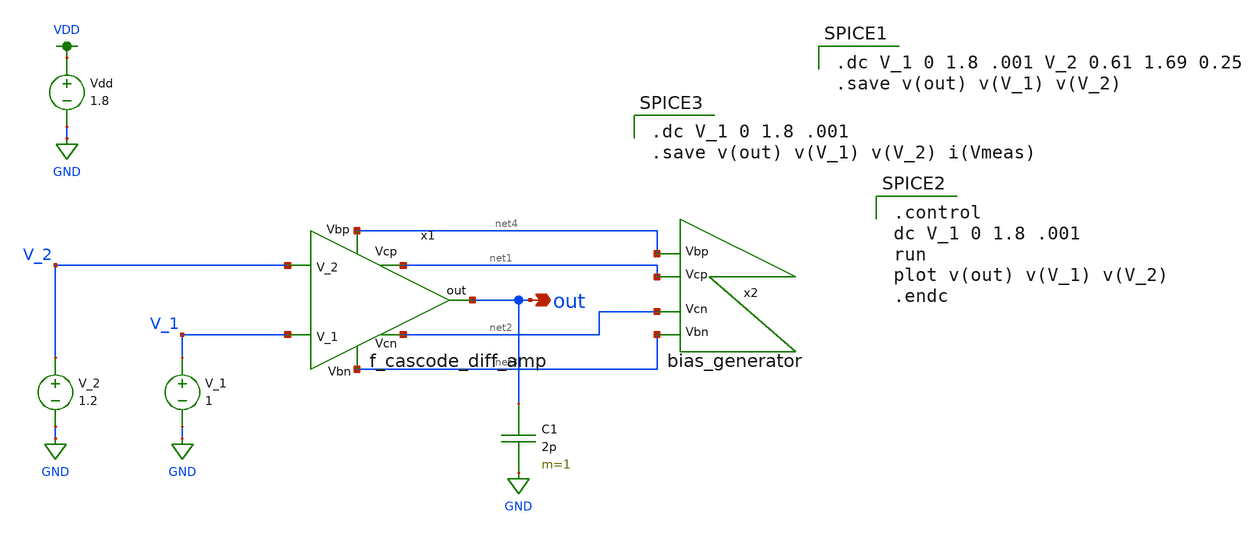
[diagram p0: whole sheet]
** sch_path: miniproject3/test_harness.sch
**.subckt test_harness out
*.opin out
x1 net4 net1 V_2 out V_1 net2 net3 f_cascode_diff_amp
x2 net4 net1 net2 net3 bias_generator
Vdd VDD GND 1.8
V_2 V_2 GND 1.2
V_1 V_1 GND 1
C1 out GND 2p m=1
**** begin user architecture code

.dc V_1 0 1.8 .001 V_2 0.61 1.69 0.25
.save v(out) v(V_1) v(V_2)


.option wnflag=1
.lib ~/skywater/skywater-pdk/libraries/sky130_fd_pr_ngspice/latest/models/sky130.lib.spice tt


.control
dc V_1 0 1.8 .001
run
plot v(out) v(V_1) v(V_2)
.endc


.dc V_1 0 1.8 .001
.save v(out) v(V_1) v(V_2) i(Vmeas)

**** end user architecture code
**.ends

* expanding   symbol:  /home/lxbtlr/MAD/miniproject3/f_cascode_diff_amp.sym # of pins=7
** sym_path: miniproject3/f_cascode_diff_amp.sym
** sch_path: miniproject3/f_cascode_diff_amp.sch
.subckt f_cascode_diff_amp Vbp Vcp V_2 out V_1 Vcn Vbn
*.ipin V_1
*.ipin V_2
*.ipin Vcp
*.ipin Vcn
*.opin out
*.ipin Vbp
*.ipin Vbn
XM11 net4 V_2 net6 GND sky130_fd_pr__nfet_01v8 L=0.5 W=12 nf=1 ad='int((nf+1)/2) * W/nf * 0.29' as='int((nf+2)/2) * W/nf * 0.29'
+ pd='2*int((nf+1)/2) * (W/nf + 0.29)' ps='2*int((nf+2)/2) * (W/nf + 0.29)' nrd='0.29 / W' nrs='0.29 / W'
+ sa=0 sb=0 sd=0 mult=1 m=1
XM10 net5 V_1 net6 GND sky130_fd_pr__nfet_01v8 L=0.5 W=12 nf=1 ad='int((nf+1)/2) * W/nf * 0.29' as='int((nf+2)/2) * W/nf * 0.29'
+ pd='2*int((nf+1)/2) * (W/nf + 0.29)' ps='2*int((nf+2)/2) * (W/nf + 0.29)' nrd='0.29 / W' nrs='0.29 / W'
+ sa=0 sb=0 sd=0 mult=1 m=1
XM1 net6 Vbn GND GND sky130_fd_pr__nfet_01v8 L=0.5 W=12 nf=1 ad='int((nf+1)/2) * W/nf * 0.29' as='int((nf+2)/2) * W/nf * 0.29'
+ pd='2*int((nf+1)/2) * (W/nf + 0.29)' ps='2*int((nf+2)/2) * (W/nf + 0.29)' nrd='0.29 / W' nrs='0.29 / W'
+ sa=0 sb=0 sd=0 mult=1 m=1
XM8 GND net2 net1 GND sky130_fd_pr__nfet_01v8 L=0.5 W=12 nf=1 ad='int((nf+1)/2) * W/nf * 0.29' as='int((nf+2)/2) * W/nf * 0.29'
+ pd='2*int((nf+1)/2) * (W/nf + 0.29)' ps='2*int((nf+2)/2) * (W/nf + 0.29)' nrd='0.29 / W' nrs='0.29 / W'
+ sa=0 sb=0 sd=0 mult=1 m=1
XM9 net3 net2 GND GND sky130_fd_pr__nfet_01v8 L=0.5 W=12 nf=1 ad='int((nf+1)/2) * W/nf * 0.29' as='int((nf+2)/2) * W/nf * 0.29'
+ pd='2*int((nf+1)/2) * (W/nf + 0.29)' ps='2*int((nf+2)/2) * (W/nf + 0.29)' nrd='0.29 / W' nrs='0.29 / W'
+ sa=0 sb=0 sd=0 mult=1 m=1
XM7 out Vcn net3 GND sky130_fd_pr__nfet_01v8 L=0.5 W=12 nf=1 ad='int((nf+1)/2) * W/nf * 0.29' as='int((nf+2)/2) * W/nf * 0.29'
+ pd='2*int((nf+1)/2) * (W/nf + 0.29)' ps='2*int((nf+2)/2) * (W/nf + 0.29)' nrd='0.29 / W' nrs='0.29 / W'
+ sa=0 sb=0 sd=0 mult=1 m=1
XM2 net2 Vcn net1 GND sky130_fd_pr__nfet_01v8 L=0.5 W=12 nf=1 ad='int((nf+1)/2) * W/nf * 0.29' as='int((nf+2)/2) * W/nf * 0.29'
+ pd='2*int((nf+1)/2) * (W/nf + 0.29)' ps='2*int((nf+2)/2) * (W/nf + 0.29)' nrd='0.29 / W' nrs='0.29 / W'
+ sa=0 sb=0 sd=0 mult=1 m=1
XM5 net2 Vcp net5 VDD sky130_fd_pr__pfet_01v8 L=0.5 W=12 nf=1 ad='int((nf+1)/2) * W/nf * 0.29' as='int((nf+2)/2) * W/nf * 0.29'
+ pd='2*int((nf+1)/2) * (W/nf + 0.29)' ps='2*int((nf+2)/2) * (W/nf + 0.29)' nrd='0.29 / W' nrs='0.29 / W'
+ sa=0 sb=0 sd=0 mult=1 m=1
XM6 out Vcp net4 VDD sky130_fd_pr__pfet_01v8 L=0.5 W=12 nf=1 ad='int((nf+1)/2) * W/nf * 0.29' as='int((nf+2)/2) * W/nf * 0.29'
+ pd='2*int((nf+1)/2) * (W/nf + 0.29)' ps='2*int((nf+2)/2) * (W/nf + 0.29)' nrd='0.29 / W' nrs='0.29 / W'
+ sa=0 sb=0 sd=0 mult=1 m=1
XM4 net4 Vbp VDD VDD sky130_fd_pr__pfet_01v8 L=0.5 W=12 nf=1 ad='int((nf+1)/2) * W/nf * 0.29' as='int((nf+2)/2) * W/nf * 0.29'
+ pd='2*int((nf+1)/2) * (W/nf + 0.29)' ps='2*int((nf+2)/2) * (W/nf + 0.29)' nrd='0.29 / W' nrs='0.29 / W'
+ sa=0 sb=0 sd=0 mult=1 m=1
XM3 net5 Vbp VDD VDD sky130_fd_pr__pfet_01v8 L=0.5 W=12 nf=1 ad='int((nf+1)/2) * W/nf * 0.29' as='int((nf+2)/2) * W/nf * 0.29'
+ pd='2*int((nf+1)/2) * (W/nf + 0.29)' ps='2*int((nf+2)/2) * (W/nf + 0.29)' nrd='0.29 / W' nrs='0.29 / W'
+ sa=0 sb=0 sd=0 mult=1 m=1
.ends


* expanding   symbol:  /home/lxbtlr/MAD/miniproject3/bias_generator.sym # of pins=4
** sym_path: miniproject3/bias_generator.sym
** sch_path: miniproject3/bias_generator.sch
.subckt bias_generator Vbp Vcp Vcn Vbn
*.opin Vbp
*.opin Vbn
*.opin Vcp
*.opin Vcn
XM1 net2 Vbp VDD VDD sky130_fd_pr__pfet_01v8 L=2.5 W=12 nf=1 ad='int((nf+1)/2) * W/nf * 0.29' as='int((nf+2)/2) * W/nf * 0.29'
+ pd='2*int((nf+1)/2) * (W/nf + 0.29)' ps='2*int((nf+2)/2) * (W/nf + 0.29)' nrd='0.29 / W' nrs='0.29 / W'
+ sa=0 sb=0 sd=0 mult=1 m=1
XM2 Vcn Vbp VDD VDD sky130_fd_pr__pfet_01v8 L=0.5 W=12 nf=1 ad='int((nf+1)/2) * W/nf * 0.29' as='int((nf+2)/2) * W/nf * 0.29'
+ pd='2*int((nf+1)/2) * (W/nf + 0.29)' ps='2*int((nf+2)/2) * (W/nf + 0.29)' nrd='0.29 / W' nrs='0.29 / W'
+ sa=0 sb=0 sd=0 mult=1 m=1
XM3 net2 net2 net1 GND sky130_fd_pr__nfet_01v8 L=0.5 W=48 nf=1 ad='int((nf+1)/2) * W/nf * 0.29' as='int((nf+2)/2) * W/nf * 0.29'
+ pd='2*int((nf+1)/2) * (W/nf + 0.29)' ps='2*int((nf+2)/2) * (W/nf + 0.29)' nrd='0.29 / W' nrs='0.29 / W'
+ sa=0 sb=0 sd=0 mult=1 m=1
XM4 net1 Vcn Vcn GND sky130_fd_pr__nfet_01v8 L=0.5 W=12 nf=1 ad='int((nf+1)/2) * W/nf * 0.29' as='int((nf+2)/2) * W/nf * 0.29'
+ pd='2*int((nf+1)/2) * (W/nf + 0.29)' ps='2*int((nf+2)/2) * (W/nf + 0.29)' nrd='0.29 / W' nrs='0.29 / W'
+ sa=0 sb=0 sd=0 mult=1 m=1
XM5 net1 net2 GND GND sky130_fd_pr__nfet_01v8 L=0.5 W=12 nf=1 ad='int((nf+1)/2) * W/nf * 0.29' as='int((nf+2)/2) * W/nf * 0.29'
+ pd='2*int((nf+1)/2) * (W/nf + 0.29)' ps='2*int((nf+2)/2) * (W/nf + 0.29)' nrd='0.29 / W' nrs='0.29 / W'
+ sa=0 sb=0 sd=0 mult=1 m=1
XM6 net4 net3 VDD VDD sky130_fd_pr__pfet_01v8 L=0.5 W=12 nf=1 ad='int((nf+1)/2) * W/nf * 0.29' as='int((nf+2)/2) * W/nf * 0.29'
+ pd='2*int((nf+1)/2) * (W/nf + 0.29)' ps='2*int((nf+2)/2) * (W/nf + 0.29)' nrd='0.29 / W' nrs='0.29 / W'
+ sa=0 sb=0 sd=0 mult=1 m=1
XM7 net3 net3 net4 VDD sky130_fd_pr__pfet_01v8 L=0.5 W=48 nf=1 ad='int((nf+1)/2) * W/nf * 0.29' as='int((nf+2)/2) * W/nf * 0.29'
+ pd='2*int((nf+1)/2) * (W/nf + 0.29)' ps='2*int((nf+2)/2) * (W/nf + 0.29)' nrd='0.29 / W' nrs='0.29 / W'
+ sa=0 sb=0 sd=0 mult=1 m=1
XM8 net4 Vcp Vcp VDD sky130_fd_pr__pfet_01v8 L=0.5 W=12 nf=1 ad='int((nf+1)/2) * W/nf * 0.29' as='int((nf+2)/2) * W/nf * 0.29'
+ pd='2*int((nf+1)/2) * (W/nf + 0.29)' ps='2*int((nf+2)/2) * (W/nf + 0.29)' nrd='0.29 / W' nrs='0.29 / W'
+ sa=0 sb=0 sd=0 mult=1 m=1
XM9 net3 Vbn GND GND sky130_fd_pr__nfet_01v8 L=2.5 W=12 nf=1 ad='int((nf+1)/2) * W/nf * 0.29' as='int((nf+2)/2) * W/nf * 0.29'
+ pd='2*int((nf+1)/2) * (W/nf + 0.29)' ps='2*int((nf+2)/2) * (W/nf + 0.29)' nrd='0.29 / W' nrs='0.29 / W'
+ sa=0 sb=0 sd=0 mult=1 m=1
XM10 Vcp Vbn GND GND sky130_fd_pr__nfet_01v8 L=0.5 W=12 nf=1 ad='int((nf+1)/2) * W/nf * 0.29' as='int((nf+2)/2) * W/nf * 0.29'
+ pd='2*int((nf+1)/2) * (W/nf + 0.29)' ps='2*int((nf+2)/2) * (W/nf + 0.29)' nrd='0.29 / W' nrs='0.29 / W'
+ sa=0 sb=0 sd=0 mult=1 m=1
I1 GND Vbn 1u
XM11 GND Vbn Vbn GND sky130_fd_pr__nfet_01v8 L=0.5 W=12 nf=1 ad='int((nf+1)/2) * W/nf * 0.29' as='int((nf+2)/2) * W/nf * 0.29'
+ pd='2*int((nf+1)/2) * (W/nf + 0.29)' ps='2*int((nf+2)/2) * (W/nf + 0.29)' nrd='0.29 / W' nrs='0.29 / W'
+ sa=0 sb=0 sd=0 mult=1 m=1
XM12 Vbp Vbn GND GND sky130_fd_pr__nfet_01v8 L=0.5 W=12 nf=1 ad='int((nf+1)/2) * W/nf * 0.29' as='int((nf+2)/2) * W/nf * 0.29'
+ pd='2*int((nf+1)/2) * (W/nf + 0.29)' ps='2*int((nf+2)/2) * (W/nf + 0.29)' nrd='0.29 / W' nrs='0.29 / W'
+ sa=0 sb=0 sd=0 mult=1 m=1
XM13 Vbp Vbp VDD VDD sky130_fd_pr__pfet_01v8 L=0.5 W=12 nf=1 ad='int((nf+1)/2) * W/nf * 0.29' as='int((nf+2)/2) * W/nf * 0.29'
+ pd='2*int((nf+1)/2) * (W/nf + 0.29)' ps='2*int((nf+2)/2) * (W/nf + 0.29)' nrd='0.29 / W' nrs='0.29 / W'
+ sa=0 sb=0 sd=0 mult=1 m=1
.ends

.GLOBAL VDD
.GLOBAL GND
.end
